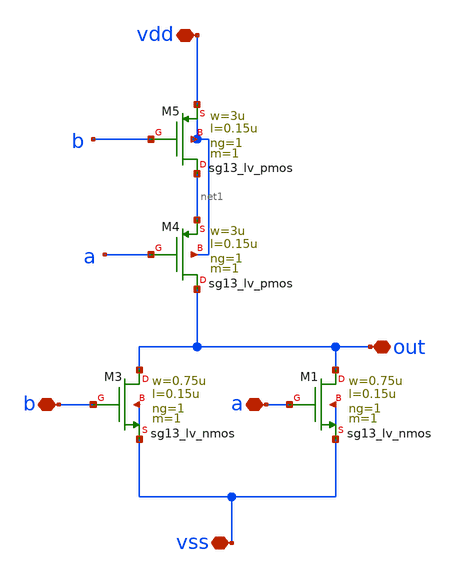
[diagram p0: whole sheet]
** sch_path: design/blocks/norgate/schematic/norgate.sch
**.subckt norgate vdd vss b a out
*.iopin vdd
*.iopin vss
*.iopin b
*.iopin a
*.iopin out
XM1 out a vss vss sg13_lv_nmos w=0.75u l=0.15u ng=1 m=1 mm_ok=1
XM4 out a net1 vdd sg13_lv_pmos w=3u l=0.15u ng=1 m=1 mm_ok=1
XM3 out b vss vss sg13_lv_nmos w=0.75u l=0.15u ng=1 m=1 mm_ok=1
XM5 net1 b vdd vdd sg13_lv_pmos w=3u l=0.15u ng=1 m=1 mm_ok=1
**.ends
.end
